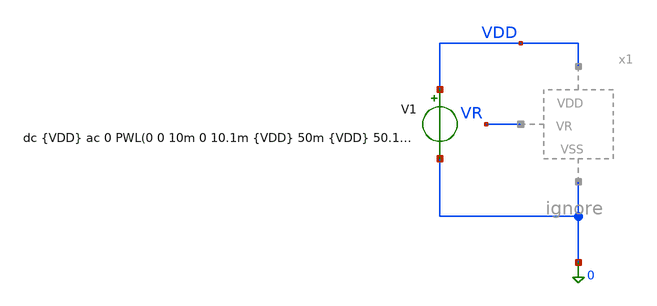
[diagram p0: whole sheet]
** sch_path: xschem/Self_Bias/self_bias_tb_pex.sch
**.subckt self_bias_tb_pex
V1 VDD 0 dc {VDD} ac 0 PWL(0 0 10m 0 10.1m {VDD} 50m {VDD} 50.1m 0 100m 0 101m {VDD} 150m {VDD} 150.1m
+ 0 200m 0 300m {VDD} 400m {VDD} 400.1m 0)
**** begin user architecture code


* ==============================================================================
* Encabezado del bloque de simulación: s1 (self_bias_tb_pex.sch)
* Descripción:
*   Testbench post-layout (PEX) para el generador de corriente auto-polarizado
*   (self_bias). Incluye 'self_bias_pex.spice', configura condiciones iniciales
*   (.nodeset) para garantizar la convergencia en .OP, mapea los transistores
*   planos extraídos por Magic (X0..X35) y restringe los vectores guardados en
*   el transitorio largo (400.1 ms) para evitar desbordamiento de memoria RAM.
* ==============================================================================

* 1. Inclusión de librería de modelos Sky130 PRIMERO y luego el netlist PEX
.lib /foss/pdks/sky130A/libs.tech/ngspice/sky130.lib.spice tt
.include /foss/designs/LDO-sky130/xschem/Self_Bias/self_bias_pex.spice
x1 VDD VR 0 self_bias

.option temp=27
.option num_threads=8
.option gmin=1e-12 reltol=1e-3 abstol=1e-12 vntol=1e-6 itl1=500 itl2=200 itl4=100

**parametros_ldo
.param VDD = 1.8

.param tstart   = 10u
.param trise    = 200u
.param tfall    = 200u
.param tsim = 'tstart+2*trise+tfall'

* Condiciones de partida en los nodos reales de self_bias_pex.spice para que
* el análisis .OP converja sin error 'Timestep too small'
.nodeset V(VR)=0.6
.nodeset V(x1.vgp_self)=1.0
.nodeset V(x1.vdi)=0.6
.nodeset V(x1.vdinv)=0.0

* Guardar por defecto únicamente las señales clave para no desbordar la RAM
* durante los 200,050 puntos del análisis transitorio (400.1 ms / 2 us)
.save v(vdd) v(vr) v(x1.vgp_self) v(x1.vdi) v(x1.vdinv) i(V1)

.control
let tstart   = 10u
let trise    = 200u
let tfall    = 200u
let tsim = '$&tstart+4*$&trise+3*$&tfall'

* --- 1. Guardar nodos y parámetros de transistores reales del PEX para .OP ---
save v(vdd) v(vr) v(x1.vgp_self) v(x1.vdi) v(x1.vdinv) i(V1)

* Mp3 (pfet_01v8_lvt rama vdi, dedo representativo X0)
save @m.x1.x0.msky130_fd_pr__pfet_01v8_lvt[gm]
save @m.x1.x0.msky130_fd_pr__pfet_01v8_lvt[gds]
save @m.x1.x0.msky130_fd_pr__pfet_01v8_lvt[id]
save @m.x1.x0.msky130_fd_pr__pfet_01v8_lvt[vgs]
save @m.x1.x0.msky130_fd_pr__pfet_01v8_lvt[vds]
save @m.x1.x0.msky130_fd_pr__pfet_01v8_lvt[vth]
save @m.x1.x0.msky130_fd_pr__pfet_01v8_lvt[vdsat]

* Mp4 (pfet_01v8_lvt rama vgp_self, dedo X2 + los 6 dedos para corriente total)
save @m.x1.x2.msky130_fd_pr__pfet_01v8_lvt[gm]
save @m.x1.x2.msky130_fd_pr__pfet_01v8_lvt[gds]
save @m.x1.x2.msky130_fd_pr__pfet_01v8_lvt[id]
save @m.x1.x2.msky130_fd_pr__pfet_01v8_lvt[vgs]
save @m.x1.x2.msky130_fd_pr__pfet_01v8_lvt[vds]
save @m.x1.x2.msky130_fd_pr__pfet_01v8_lvt[vth]
save @m.x1.x2.msky130_fd_pr__pfet_01v8_lvt[vdsat]
save @m.x1.x7.msky130_fd_pr__pfet_01v8_lvt[id]
save @m.x1.x11.msky130_fd_pr__pfet_01v8_lvt[id]
save @m.x1.x14.msky130_fd_pr__pfet_01v8_lvt[id]
save @m.x1.x16.msky130_fd_pr__pfet_01v8_lvt[id]
save @m.x1.x19.msky130_fd_pr__pfet_01v8_lvt[id]

* Ms1 (nfet_01v8 de arranque, dedo representativo X13)
save @m.x1.x13.msky130_fd_pr__nfet_01v8[gm]
save @m.x1.x13.msky130_fd_pr__nfet_01v8[gds]
save @m.x1.x13.msky130_fd_pr__nfet_01v8[id]
save @m.x1.x13.msky130_fd_pr__nfet_01v8[vgs]
save @m.x1.x13.msky130_fd_pr__nfet_01v8[vds]
save @m.x1.x13.msky130_fd_pr__nfet_01v8[vth]
save @m.x1.x13.msky130_fd_pr__nfet_01v8[vdsat]

* Ms3 (nfet_01v8 de arranque, dedo representativo X6)
save @m.x1.x6.msky130_fd_pr__nfet_01v8[gm]
save @m.x1.x6.msky130_fd_pr__nfet_01v8[gds]
save @m.x1.x6.msky130_fd_pr__nfet_01v8[id]
save @m.x1.x6.msky130_fd_pr__nfet_01v8[vgs]
save @m.x1.x6.msky130_fd_pr__nfet_01v8[vds]
save @m.x1.x6.msky130_fd_pr__nfet_01v8[vth]
save @m.x1.x6.msky130_fd_pr__nfet_01v8[vdsat]

* Mn1 (nfet_01v8 espejo inferior, dedo representativo X23)
save @m.x1.x23.msky130_fd_pr__nfet_01v8[gm]
save @m.x1.x23.msky130_fd_pr__nfet_01v8[gds]
save @m.x1.x23.msky130_fd_pr__nfet_01v8[id]
save @m.x1.x23.msky130_fd_pr__nfet_01v8[vgs]
save @m.x1.x23.msky130_fd_pr__nfet_01v8[vds]
save @m.x1.x23.msky130_fd_pr__nfet_01v8[vth]
save @m.x1.x23.msky130_fd_pr__nfet_01v8[vdsat]

* Mn2 (nfet_01v8 conectado a R_iref, dedo representativo X1)
save @m.x1.x1.msky130_fd_pr__nfet_01v8[gm]
save @m.x1.x1.msky130_fd_pr__nfet_01v8[gds]
save @m.x1.x1.msky130_fd_pr__nfet_01v8[id]
save @m.x1.x1.msky130_fd_pr__nfet_01v8[vgs]
save @m.x1.x1.msky130_fd_pr__nfet_01v8[vds]
save @m.x1.x1.msky130_fd_pr__nfet_01v8[vth]
save @m.x1.x1.msky130_fd_pr__nfet_01v8[vdsat]

set filetype=ascii
op
write self_bias_pex_tb.raw

* 2. Calcular VR e Ibias total (suma de los 6 dedos de Mp4 en microamperios)
let vr_op = v(vr)
let ibias_val_uA_op = (@m.x1.x2.msky130_fd_pr__pfet_01v8_lvt[id] +
+ @m.x1.x7.msky130_fd_pr__pfet_01v8_lvt[id] + @m.x1.x11.msky130_fd_pr__pfet_01v8_lvt[id] + @m.x1.x14.msky130_fd_pr__pfet_01v8_lvt[id] +
+ @m.x1.x16.msky130_fd_pr__pfet_01v8_lvt[id] + @m.x1.x19.msky130_fd_pr__pfet_01v8_lvt[id]) * 1e6

echo VR = $&vr_op
echo ibias = $&ibias_val_uA_op uA

* 3. Reiniciar y guardar SOLO los nodos principales antes del transitorio largo
reset
save v(vdd) v(vr) v(x1.vgp_self) v(x1.vdi) v(x1.vdinv) i(V1)

tran 2u 400.1m

* --- 4. Mediciones del Start-up ---
* Para Trise = 100us (Pulso activo entre 10m y 50m)
meas tran vr_100us FIND v(vr) at=40m

* Para Trise = 1ms (Pulso activo entre 100m y 150m)
meas tran vr_1ms FIND v(vr) at=140m

* Para Trise = 100ms (Pulso activo entre 200m y 400m)
meas tran vr_100ms FIND v(vr) at=390m

print vr_100us vr_1ms vr_100ms

.endc



**** end user architecture code
**.ends
.end
